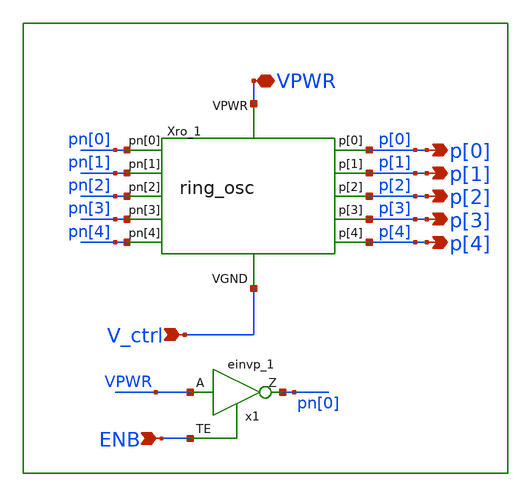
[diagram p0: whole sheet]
** sch_path: circuit/library/vco.sch
**.subckt vco VPWR p[0] ENB p[1] p[2] p[3] p[4] V_ctrl
*.iopin VPWR
*.opin p[0]
*.ipin ENB
*.opin p[1]
*.opin p[2]
*.opin p[3]
*.opin p[4]
*.ipin V_ctrl
x1 VPWR ENB VGND VNB VPB VPWR pn[0] sky130_fd_sc_hd__einvp_1
Xro_1 VPWR p[1] p[3] p[0] p[4] p[2] pn[0] pn[2] pn[1] pn[3] pn[4] V_ctrl ring_osc L12="L12"
+ Wp12="Wp12" Wn12="Wn12" L34="L34" Wp34="Wp34" Wn34="Wn34"
**.ends
.end
